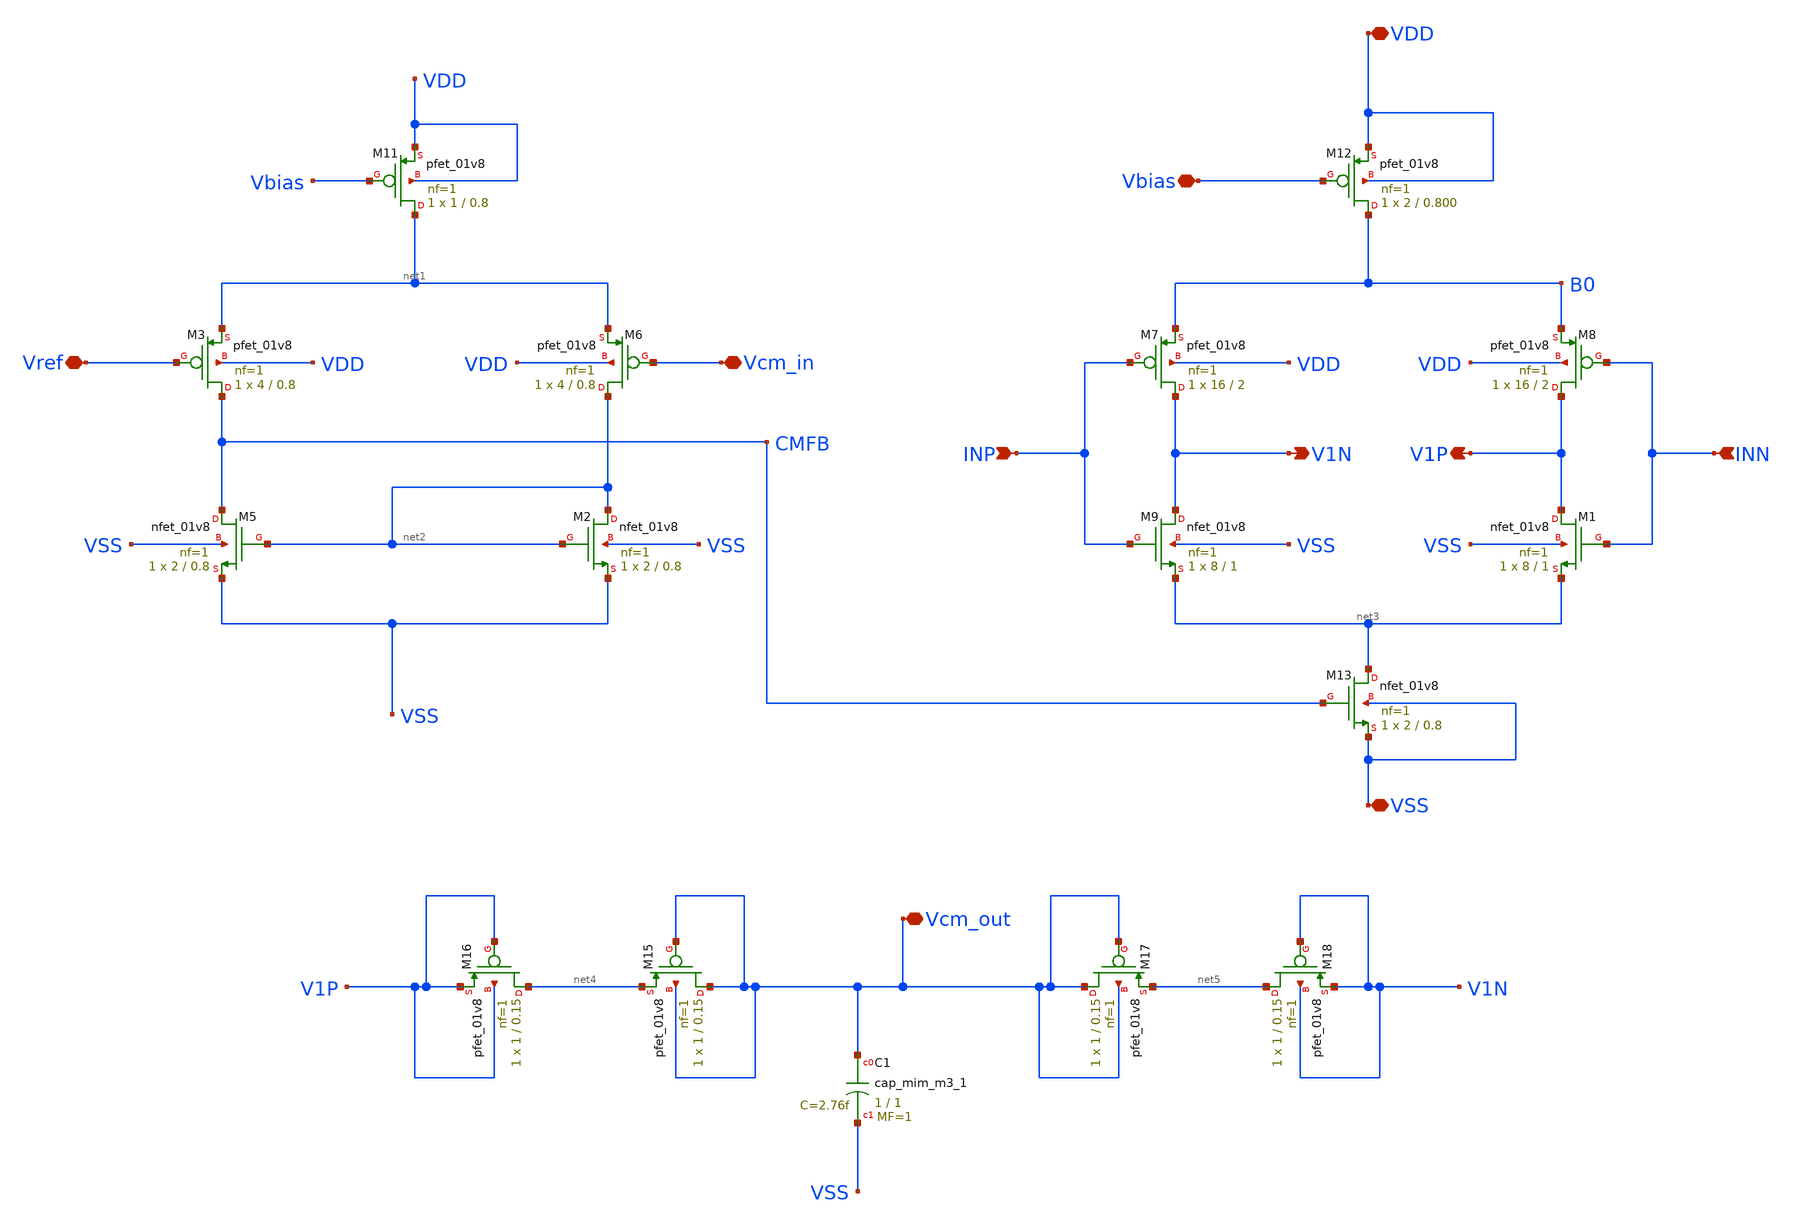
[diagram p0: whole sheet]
** sch_path: opamp_lna/low_noise_amp.sch
**.subckt low_noise_amp VDD VSS Vbias INP INN Vref Vcm_in Vcm_out V1N V1P
*.iopin VDD
*.iopin VSS
*.iopin Vbias
*.ipin INP
*.ipin INN
*.iopin Vref
*.iopin Vcm_in
*.iopin Vcm_out
*.opin V1N
*.opin V1P
XM3 CMFB Vref net1 VDD sky130_fd_pr__pfet_01v8 L=0.8 W=4 nf=1 ad='int((nf+1)/2) * W/nf * 0.29' as='int((nf+2)/2) * W/nf * 0.29'
+ pd='2*int((nf+1)/2) * (W/nf + 0.29)' ps='2*int((nf+2)/2) * (W/nf + 0.29)' nrd='0.29 / W' nrs='0.29 / W'
+ sa=0 sb=0 sd=0 mult=1 m=1
XM11 net1 Vbias VDD VDD sky130_fd_pr__pfet_01v8 L=0.8 W=1 nf=1 ad='int((nf+1)/2) * W/nf * 0.29' as='int((nf+2)/2) * W/nf * 0.29'
+ pd='2*int((nf+1)/2) * (W/nf + 0.29)' ps='2*int((nf+2)/2) * (W/nf + 0.29)' nrd='0.29 / W' nrs='0.29 / W'
+ sa=0 sb=0 sd=0 mult=1 m=1
XM7 V1N INP B0 VDD sky130_fd_pr__pfet_01v8 L=2 W=16 nf=1 ad='int((nf+1)/2) * W/nf * 0.29' as='int((nf+2)/2) * W/nf * 0.29'
+ pd='2*int((nf+1)/2) * (W/nf + 0.29)' ps='2*int((nf+2)/2) * (W/nf + 0.29)' nrd='0.29 / W' nrs='0.29 / W'
+ sa=0 sb=0 sd=0 mult=1 m=1
XM8 V1P INN B0 VDD sky130_fd_pr__pfet_01v8 L=2 W=16 nf=1 ad='int((nf+1)/2) * W/nf * 0.29' as='int((nf+2)/2) * W/nf * 0.29'
+ pd='2*int((nf+1)/2) * (W/nf + 0.29)' ps='2*int((nf+2)/2) * (W/nf + 0.29)' nrd='0.29 / W' nrs='0.29 / W'
+ sa=0 sb=0 sd=0 mult=1 m=1
XM9 V1N INP net3 VSS sky130_fd_pr__nfet_01v8 L=1 W=8 nf=1 ad='int((nf+1)/2) * W/nf * 0.29' as='int((nf+2)/2) * W/nf * 0.29'
+ pd='2*int((nf+1)/2) * (W/nf + 0.29)' ps='2*int((nf+2)/2) * (W/nf + 0.29)' nrd='0.29 / W' nrs='0.29 / W'
+ sa=0 sb=0 sd=0 mult=1 m=1
XM12 B0 Vbias VDD VDD sky130_fd_pr__pfet_01v8 L=0.800 W=2 nf=1 ad='int((nf+1)/2) * W/nf * 0.29' as='int((nf+2)/2) * W/nf * 0.29'
+ pd='2*int((nf+1)/2) * (W/nf + 0.29)' ps='2*int((nf+2)/2) * (W/nf + 0.29)' nrd='0.29 / W' nrs='0.29 / W'
+ sa=0 sb=0 sd=0 mult=1 m=1
XM13 net3 CMFB VSS VSS sky130_fd_pr__nfet_01v8 L=0.8 W=2 nf=1 ad='int((nf+1)/2) * W/nf * 0.29' as='int((nf+2)/2) * W/nf * 0.29'
+ pd='2*int((nf+1)/2) * (W/nf + 0.29)' ps='2*int((nf+2)/2) * (W/nf + 0.29)' nrd='0.29 / W' nrs='0.29 / W'
+ sa=0 sb=0 sd=0 mult=1 m=1
XM15 Vcm_out Vcm_out net4 Vcm_out sky130_fd_pr__pfet_01v8 L=0.15 W=1 nf=1 ad='int((nf+1)/2) * W/nf * 0.29'
+ as='int((nf+2)/2) * W/nf * 0.29' pd='2*int((nf+1)/2) * (W/nf + 0.29)' ps='2*int((nf+2)/2) * (W/nf + 0.29)'
+ nrd='0.29 / W' nrs='0.29 / W' sa=0 sb=0 sd=0 mult=1 m=1
XM16 net4 V1P V1P V1P sky130_fd_pr__pfet_01v8 L=0.15 W=1 nf=1 ad='int((nf+1)/2) * W/nf * 0.29' as='int((nf+2)/2) * W/nf * 0.29'
+ pd='2*int((nf+1)/2) * (W/nf + 0.29)' ps='2*int((nf+2)/2) * (W/nf + 0.29)' nrd='0.29 / W' nrs='0.29 / W'
+ sa=0 sb=0 sd=0 mult=1 m=1
XM17 Vcm_out Vcm_out net5 Vcm_out sky130_fd_pr__pfet_01v8 L=0.15 W=1 nf=1 ad='int((nf+1)/2) * W/nf * 0.29'
+ as='int((nf+2)/2) * W/nf * 0.29' pd='2*int((nf+1)/2) * (W/nf + 0.29)' ps='2*int((nf+2)/2) * (W/nf + 0.29)'
+ nrd='0.29 / W' nrs='0.29 / W' sa=0 sb=0 sd=0 mult=1 m=1
XM18 net5 V1N V1N V1N sky130_fd_pr__pfet_01v8 L=0.15 W=1 nf=1 ad='int((nf+1)/2) * W/nf * 0.29' as='int((nf+2)/2) * W/nf * 0.29'
+ pd='2*int((nf+1)/2) * (W/nf + 0.29)' ps='2*int((nf+2)/2) * (W/nf + 0.29)' nrd='0.29 / W' nrs='0.29 / W'
+ sa=0 sb=0 sd=0 mult=1 m=1
XC1 Vcm_out VSS sky130_fd_pr__cap_mim_m3_1 W=1 L=1 MF=1 m=1
XM1 V1P INN net3 VSS sky130_fd_pr__nfet_01v8 L=1 W=8 nf=1 ad='int((nf+1)/2) * W/nf * 0.29' as='int((nf+2)/2) * W/nf * 0.29'
+ pd='2*int((nf+1)/2) * (W/nf + 0.29)' ps='2*int((nf+2)/2) * (W/nf + 0.29)' nrd='0.29 / W' nrs='0.29 / W'
+ sa=0 sb=0 sd=0 mult=1 m=1
XM2 net2 net2 VSS VSS sky130_fd_pr__nfet_01v8 L=0.8 W=2 nf=1 ad='int((nf+1)/2) * W/nf * 0.29' as='int((nf+2)/2) * W/nf * 0.29'
+ pd='2*int((nf+1)/2) * (W/nf + 0.29)' ps='2*int((nf+2)/2) * (W/nf + 0.29)' nrd='0.29 / W' nrs='0.29 / W'
+ sa=0 sb=0 sd=0 mult=1 m=1
XM5 CMFB net2 VSS VSS sky130_fd_pr__nfet_01v8 L=0.8 W=2 nf=1 ad='int((nf+1)/2) * W/nf * 0.29' as='int((nf+2)/2) * W/nf * 0.29'
+ pd='2*int((nf+1)/2) * (W/nf + 0.29)' ps='2*int((nf+2)/2) * (W/nf + 0.29)' nrd='0.29 / W' nrs='0.29 / W'
+ sa=0 sb=0 sd=0 mult=1 m=1
XM6 net2 Vcm_in net1 VDD sky130_fd_pr__pfet_01v8 L=0.8 W=4 nf=1 ad='int((nf+1)/2) * W/nf * 0.29' as='int((nf+2)/2) * W/nf * 0.29'
+ pd='2*int((nf+1)/2) * (W/nf + 0.29)' ps='2*int((nf+2)/2) * (W/nf + 0.29)' nrd='0.29 / W' nrs='0.29 / W'
+ sa=0 sb=0 sd=0 mult=1 m=1
**.ends
.end
